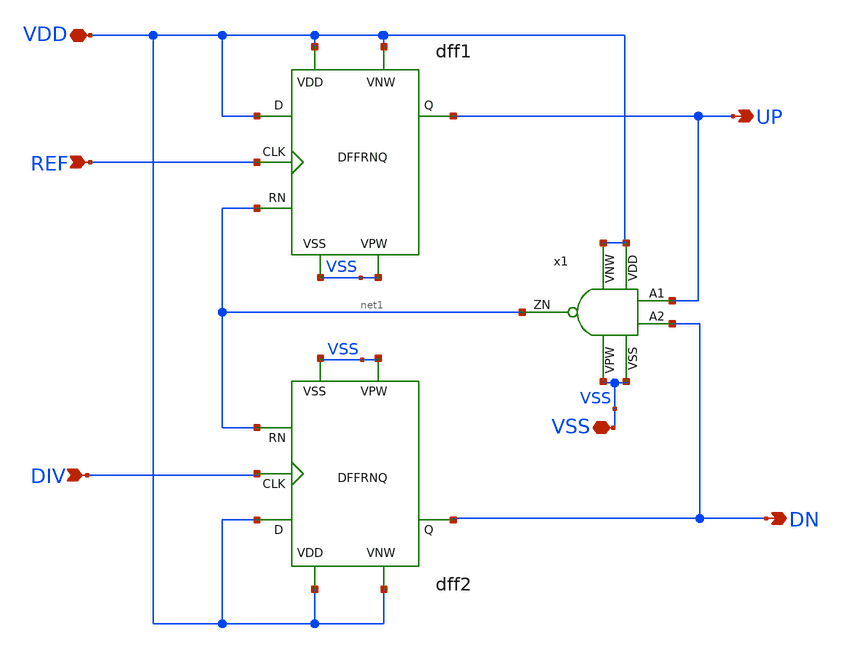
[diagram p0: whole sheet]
** sch_path: src/UN_PFD_GF180mcuD/work/UN_PFD_UD_GF180mcuD.sch
**.subckt UN_PFD_UD_GF180mcuD REF DIV VDD VSS UP DN
*.ipin REF
*.ipin DIV
*.iopin VDD
*.iopin VSS
*.opin UP
*.opin DN
dff1 VDD VDD net1 VSS UP REF VSS VDD UN_DFFRNQ_1_GF180mcuD
dff2 VDD VDD net1 net2 DN net3 net4 VDD UN_DFFRNQ_1_GF180mcuD
x1 DN UP net5 VDD net6 net7 net1 UN_NAND2_0_GF180mcuD
**.ends
.end
